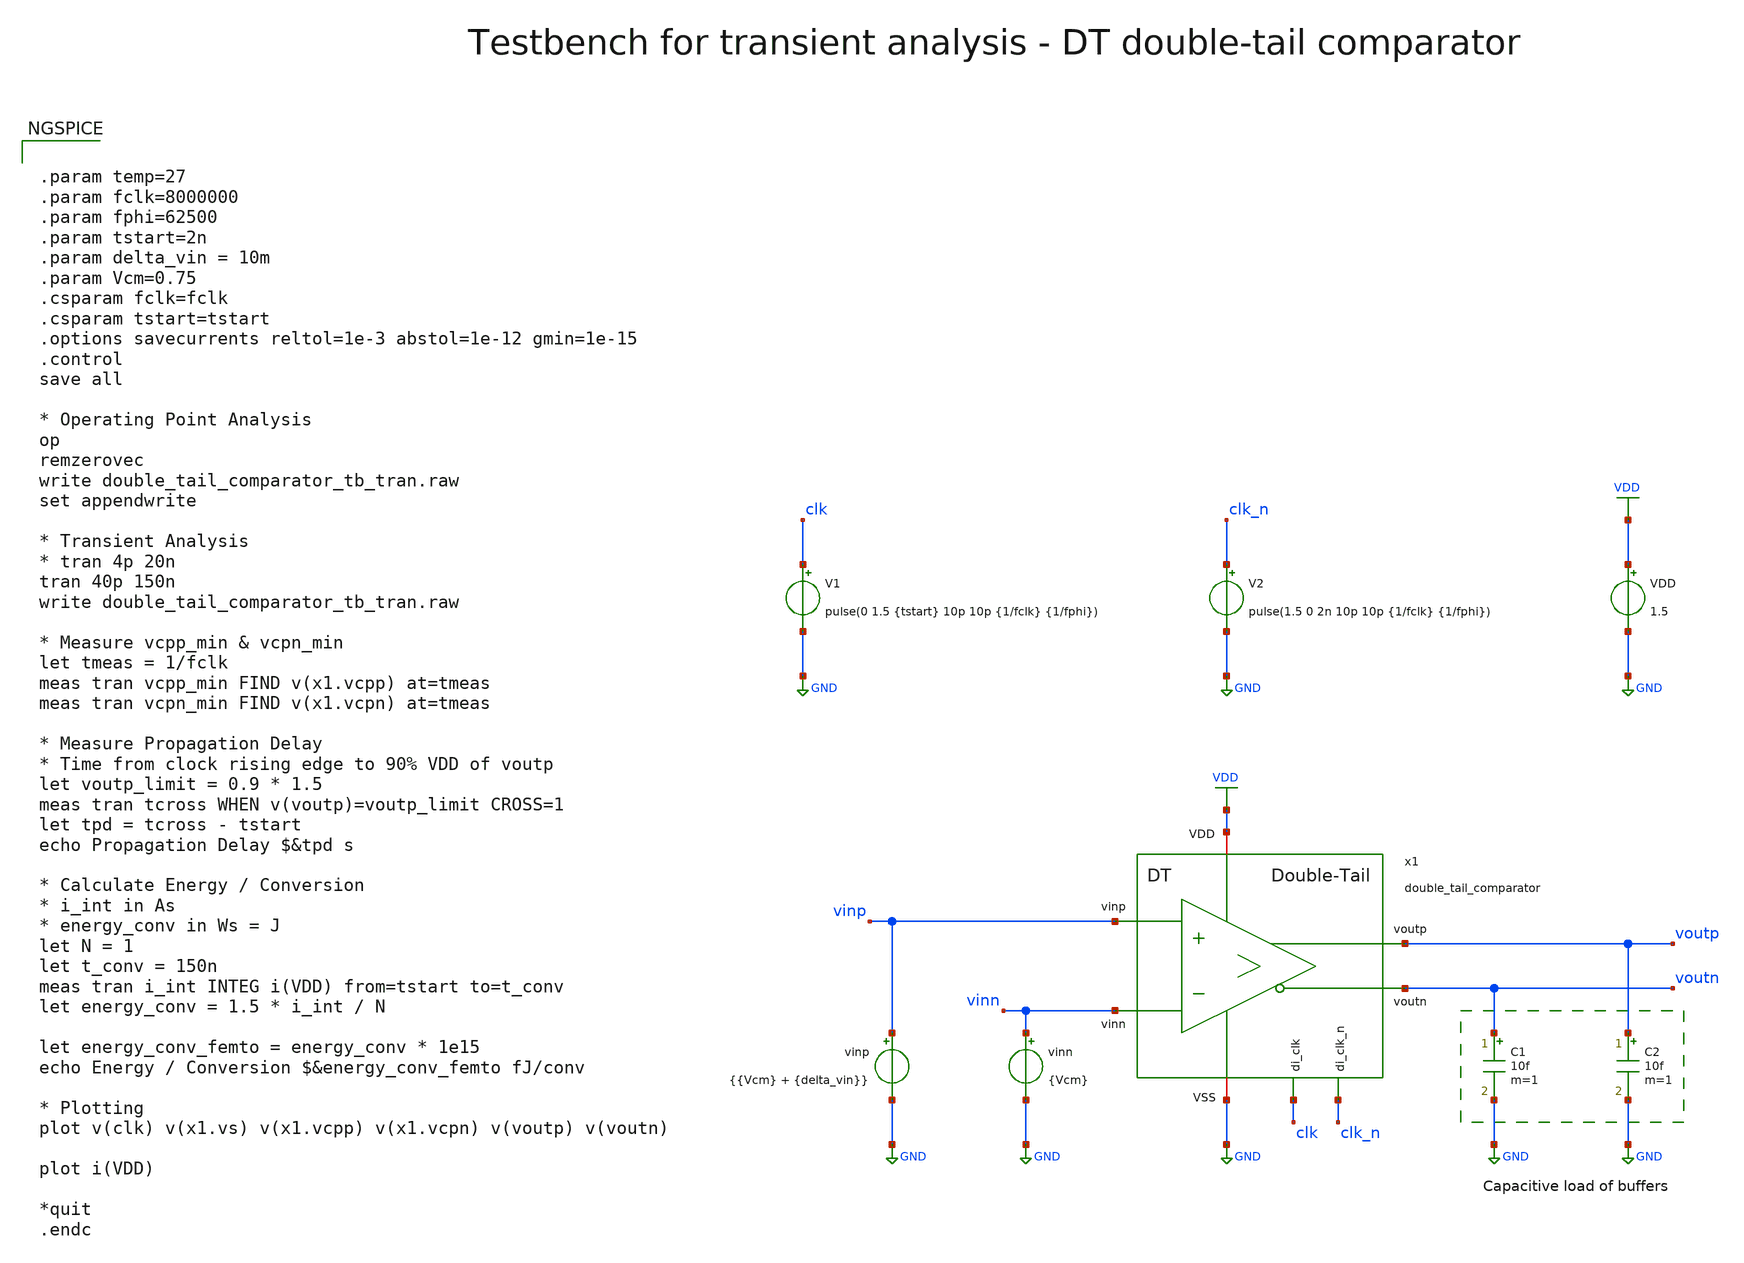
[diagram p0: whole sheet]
** sch_path: SG13G2_ATBS-ADC-main/xschem/comparator/discrete_time/Double-tail/testbenches/double_tail_comparator_tb_tran.sch
**.subckt double_tail_comparator_tb_tran
VDD VDD GND 1.5
V1 clk GND pulse(0 1.5 {tstart} 10p 10p {1/fclk} {1/fphi})
vinn vinn GND {Vcm}
vinp vinp GND {{Vcm} + {delta_vin}}
V2 clk_n GND pulse(1.5 0 2n 10p 10p {1/fclk} {1/fphi})
C1 voutn GND 10f m=1
C2 voutp GND 10f m=1
x1 clk_n clk VDD voutp vinp GND voutn vinn double_tail_comparator
**** begin user architecture code

.lib cornerMOSlv.lib mos_tt
.lib cornerMOShv.lib mos_tt
.lib cornerRES.lib res_typ



.param temp=27
.param fclk=8000000
.param fphi=62500
.param tstart=2n
.param delta_vin = 10m
.param Vcm=0.75
.csparam fclk=fclk
.csparam tstart=tstart
.options savecurrents reltol=1e-3 abstol=1e-12 gmin=1e-15
.control
save all

* Operating Point Analysis
op
remzerovec
write double_tail_comparator_tb_tran.raw
set appendwrite

* Transient Analysis
* tran 4p 20n
tran 40p 150n
write double_tail_comparator_tb_tran.raw

* Measure vcpp_min & vcpn_min
let tmeas = 1/fclk
meas tran vcpp_min FIND v(x1.vcpp) at=tmeas
meas tran vcpn_min FIND v(x1.vcpn) at=tmeas

* Measure Propagation Delay
* Time from clock rising edge to 90% VDD of voutp
let voutp_limit = 0.9 * 1.5
meas tran tcross WHEN v(voutp)=voutp_limit CROSS=1
let tpd = tcross - tstart
echo Propagation Delay $&tpd s

* Calculate Energy / Conversion
* i_int in As
* energy_conv in Ws = J
let N = 1
let t_conv = 150n
meas tran i_int INTEG i(VDD) from=tstart to=t_conv
let energy_conv = 1.5 * i_int / N

let energy_conv_femto = energy_conv * 1e15
echo Energy / Conversion $&energy_conv_femto fJ/conv

* Plotting
plot v(clk) v(x1.vs) v(x1.vcpp) v(x1.vcpn) v(voutp) v(voutn)

plot i(VDD)

*quit
.endc

**** end user architecture code
**.ends

* expanding   symbol:  comparator/discrete_time/Double-tail/double_tail_comparator.sym # of pins=8
** sym_path: SG13G2_ATBS-ADC-main/xschem/comparator/discrete_time/Double-tail/double_tail_comparator.sym
** sch_path: SG13G2_ATBS-ADC-main/xschem/comparator/discrete_time/Double-tail/double_tail_comparator.sch
.subckt double_tail_comparator di_clk_n di_clk VDD voutp vinp VSS voutn vinn
*.opin voutp
*.opin voutn
*.ipin di_clk_n
*.iopin VDD
*.iopin VSS
*.ipin vinp
*.ipin vinn
*.ipin di_clk
XM6 voutp vcpn VSS VSS sg13_lv_nmos w=1.0u l=0.13u ng=1 m=1 mm_ok=1
XM8 net1 di_clk_n VDD VDD sg13_lv_pmos w=2.0u l=0.13u ng=2 m=1 mm_ok=1
XM9 voutp voutn net1 VDD sg13_lv_pmos w=2.0u l=0.13u ng=2 m=1 mm_ok=1
XM10 voutn voutp net1 VDD sg13_lv_pmos w=2.0u l=0.13u ng=2 m=1 mm_ok=1
XM11 voutp voutn VSS VSS sg13_lv_nmos w=1.0u l=0.13u ng=1 m=1 mm_ok=1
XM12 voutn voutp VSS VSS sg13_lv_nmos w=1.0u l=0.13u ng=1 m=1 mm_ok=1
XM7 voutn vcpp VSS VSS sg13_lv_nmos w=1.0u l=0.13u ng=1 m=1 mm_ok=1
CP1 vcpn VSS 300f m=1
CP2 vcpp VSS 300f m=1
XM1 vcpn vinp vs VSS sg13_lv_nmos w=1.0u l=0.13u ng=1 m=1 mm_ok=1
XM2 vcpp vinn vs VSS sg13_lv_nmos w=1.0u l=0.13u ng=1 m=1 mm_ok=1
XM3 vs di_clk VSS VSS sg13_lv_nmos w=1.0u l=0.13u ng=1 m=1 mm_ok=1
XM4 vcpn di_clk VDD VDD sg13_lv_pmos w=1.0u l=0.13u ng=1 m=1 mm_ok=1
XM5 vcpp di_clk VDD VDD sg13_lv_pmos w=1.0u l=0.13u ng=1 m=1 mm_ok=1
.ends

.GLOBAL GND
.GLOBAL VDD
.end
